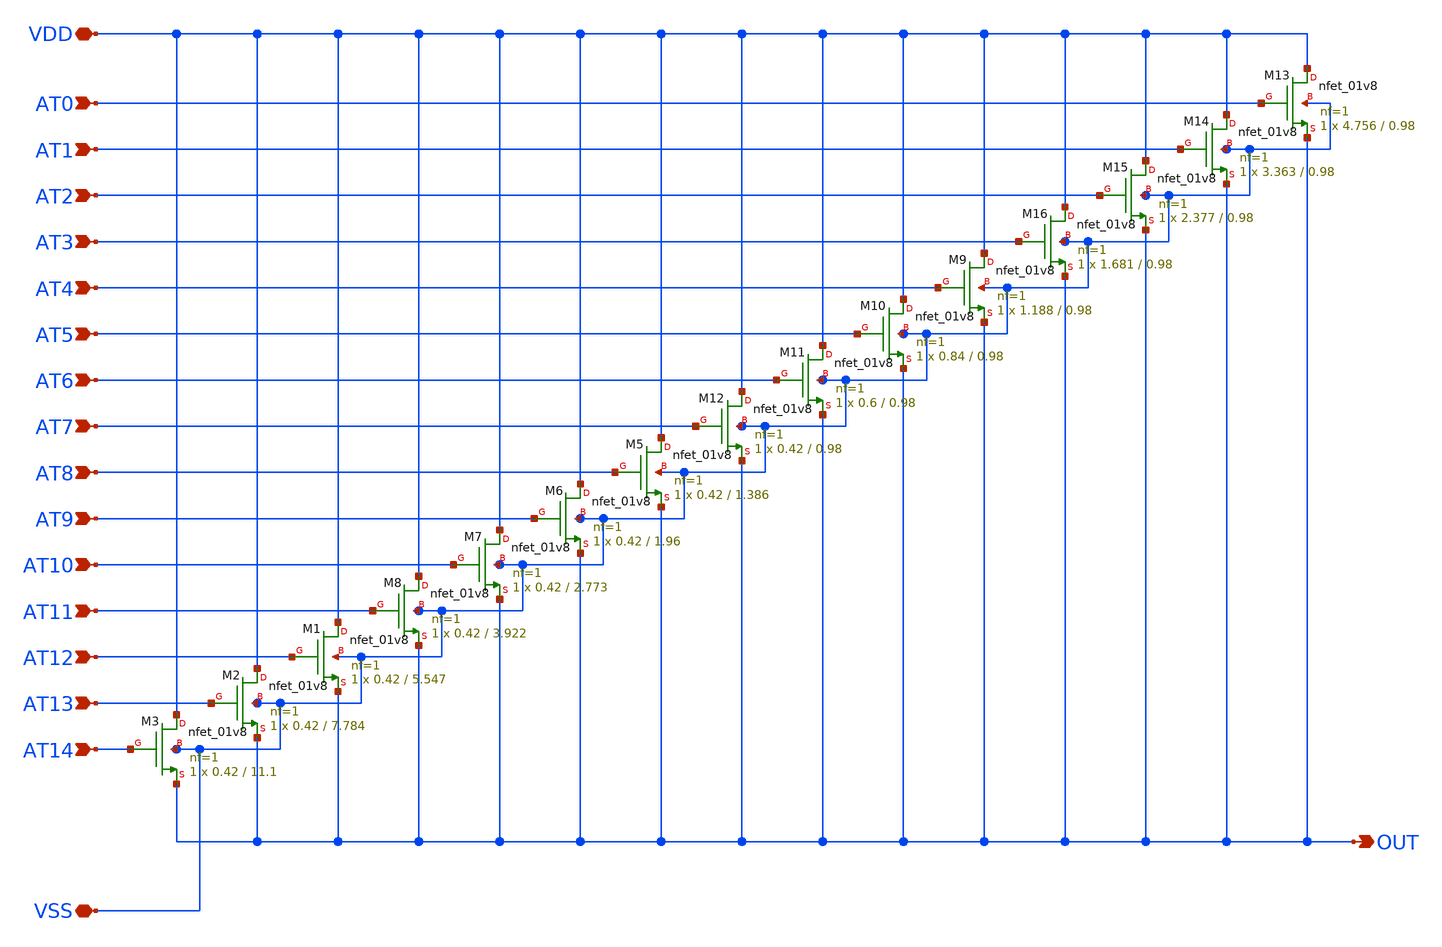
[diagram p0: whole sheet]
** sch_path: xschem/dac_16nfet.sch
**.subckt dac_16nfet AT12 AT13 VDD VSS OUT AT14 AT4 AT5 AT6 AT7 AT8 AT9 AT10 AT11 AT0 AT1 AT2 AT3
*.ipin AT12
*.ipin AT13
*.iopin VDD
*.iopin VSS
*.opin OUT
*.ipin AT14
*.ipin AT4
*.ipin AT5
*.ipin AT6
*.ipin AT7
*.ipin AT8
*.ipin AT9
*.ipin AT10
*.ipin AT11
*.ipin AT0
*.ipin AT1
*.ipin AT2
*.ipin AT3
XM1 VDD AT12 OUT VSS sky130_fd_pr__nfet_01v8 L=5.547 W=0.42 nf=1 ad='int((nf+1)/2) * W/nf * 0.29' as='int((nf+2)/2) * W/nf * 0.29'
+ pd='2*int((nf+1)/2) * (W/nf + 0.29)' ps='2*int((nf+2)/2) * (W/nf + 0.29)' nrd='0.29 / W' nrs='0.29 / W'
+ sa=0 sb=0 sd=0 mult=1 m=1
XM2 VDD AT13 OUT VSS sky130_fd_pr__nfet_01v8 L=7.784 W=0.42 nf=1 ad='int((nf+1)/2) * W/nf * 0.29' as='int((nf+2)/2) * W/nf * 0.29'
+ pd='2*int((nf+1)/2) * (W/nf + 0.29)' ps='2*int((nf+2)/2) * (W/nf + 0.29)' nrd='0.29 / W' nrs='0.29 / W'
+ sa=0 sb=0 sd=0 mult=1 m=1
XM3 VDD AT14 OUT VSS sky130_fd_pr__nfet_01v8 L=11.1 W=0.42 nf=1 ad='int((nf+1)/2) * W/nf * 0.29' as='int((nf+2)/2) * W/nf * 0.29'
+ pd='2*int((nf+1)/2) * (W/nf + 0.29)' ps='2*int((nf+2)/2) * (W/nf + 0.29)' nrd='0.29 / W' nrs='0.29 / W'
+ sa=0 sb=0 sd=0 mult=1 m=1
XM5 VDD AT8 OUT VSS sky130_fd_pr__nfet_01v8 L=1.386 W=0.42 nf=1 ad='int((nf+1)/2) * W/nf * 0.29' as='int((nf+2)/2) * W/nf * 0.29'
+ pd='2*int((nf+1)/2) * (W/nf + 0.29)' ps='2*int((nf+2)/2) * (W/nf + 0.29)' nrd='0.29 / W' nrs='0.29 / W'
+ sa=0 sb=0 sd=0 mult=1 m=1
XM6 VDD AT9 OUT VSS sky130_fd_pr__nfet_01v8 L=1.96 W=0.42 nf=1 ad='int((nf+1)/2) * W/nf * 0.29' as='int((nf+2)/2) * W/nf * 0.29'
+ pd='2*int((nf+1)/2) * (W/nf + 0.29)' ps='2*int((nf+2)/2) * (W/nf + 0.29)' nrd='0.29 / W' nrs='0.29 / W'
+ sa=0 sb=0 sd=0 mult=1 m=1
XM7 VDD AT10 OUT VSS sky130_fd_pr__nfet_01v8 L=2.773 W=0.42 nf=1 ad='int((nf+1)/2) * W/nf * 0.29' as='int((nf+2)/2) * W/nf * 0.29'
+ pd='2*int((nf+1)/2) * (W/nf + 0.29)' ps='2*int((nf+2)/2) * (W/nf + 0.29)' nrd='0.29 / W' nrs='0.29 / W'
+ sa=0 sb=0 sd=0 mult=1 m=1
XM8 VDD AT11 OUT VSS sky130_fd_pr__nfet_01v8 L=3.922 W=0.42 nf=1 ad='int((nf+1)/2) * W/nf * 0.29' as='int((nf+2)/2) * W/nf * 0.29'
+ pd='2*int((nf+1)/2) * (W/nf + 0.29)' ps='2*int((nf+2)/2) * (W/nf + 0.29)' nrd='0.29 / W' nrs='0.29 / W'
+ sa=0 sb=0 sd=0 mult=1 m=1
XM9 VDD AT4 OUT VSS sky130_fd_pr__nfet_01v8 L=0.98 W=1.188 nf=1 ad='int((nf+1)/2) * W/nf * 0.29' as='int((nf+2)/2) * W/nf * 0.29'
+ pd='2*int((nf+1)/2) * (W/nf + 0.29)' ps='2*int((nf+2)/2) * (W/nf + 0.29)' nrd='0.29 / W' nrs='0.29 / W'
+ sa=0 sb=0 sd=0 mult=1 m=1
XM10 VDD AT5 OUT VSS sky130_fd_pr__nfet_01v8 L=0.98 W=0.84 nf=1 ad='int((nf+1)/2) * W/nf * 0.29' as='int((nf+2)/2) * W/nf * 0.29'
+ pd='2*int((nf+1)/2) * (W/nf + 0.29)' ps='2*int((nf+2)/2) * (W/nf + 0.29)' nrd='0.29 / W' nrs='0.29 / W'
+ sa=0 sb=0 sd=0 mult=1 m=1
XM11 VDD AT6 OUT VSS sky130_fd_pr__nfet_01v8 L=0.98 W=0.6 nf=1 ad='int((nf+1)/2) * W/nf * 0.29' as='int((nf+2)/2) * W/nf * 0.29'
+ pd='2*int((nf+1)/2) * (W/nf + 0.29)' ps='2*int((nf+2)/2) * (W/nf + 0.29)' nrd='0.29 / W' nrs='0.29 / W'
+ sa=0 sb=0 sd=0 mult=1 m=1
XM12 VDD AT7 OUT VSS sky130_fd_pr__nfet_01v8 L=0.98 W=0.42 nf=1 ad='int((nf+1)/2) * W/nf * 0.29' as='int((nf+2)/2) * W/nf * 0.29'
+ pd='2*int((nf+1)/2) * (W/nf + 0.29)' ps='2*int((nf+2)/2) * (W/nf + 0.29)' nrd='0.29 / W' nrs='0.29 / W'
+ sa=0 sb=0 sd=0 mult=1 m=1
XM13 VDD AT0 OUT VSS sky130_fd_pr__nfet_01v8 L=0.98 W=4.756 nf=1 ad='int((nf+1)/2) * W/nf * 0.29' as='int((nf+2)/2) * W/nf * 0.29'
+ pd='2*int((nf+1)/2) * (W/nf + 0.29)' ps='2*int((nf+2)/2) * (W/nf + 0.29)' nrd='0.29 / W' nrs='0.29 / W'
+ sa=0 sb=0 sd=0 mult=1 m=1
XM14 VDD AT1 OUT VSS sky130_fd_pr__nfet_01v8 L=0.98 W=3.363 nf=1 ad='int((nf+1)/2) * W/nf * 0.29' as='int((nf+2)/2) * W/nf * 0.29'
+ pd='2*int((nf+1)/2) * (W/nf + 0.29)' ps='2*int((nf+2)/2) * (W/nf + 0.29)' nrd='0.29 / W' nrs='0.29 / W'
+ sa=0 sb=0 sd=0 mult=1 m=1
XM15 VDD AT2 OUT VSS sky130_fd_pr__nfet_01v8 L=0.98 W=2.377 nf=1 ad='int((nf+1)/2) * W/nf * 0.29' as='int((nf+2)/2) * W/nf * 0.29'
+ pd='2*int((nf+1)/2) * (W/nf + 0.29)' ps='2*int((nf+2)/2) * (W/nf + 0.29)' nrd='0.29 / W' nrs='0.29 / W'
+ sa=0 sb=0 sd=0 mult=1 m=1
XM16 VDD AT3 OUT VSS sky130_fd_pr__nfet_01v8 L=0.98 W=1.681 nf=1 ad='int((nf+1)/2) * W/nf * 0.29' as='int((nf+2)/2) * W/nf * 0.29'
+ pd='2*int((nf+1)/2) * (W/nf + 0.29)' ps='2*int((nf+2)/2) * (W/nf + 0.29)' nrd='0.29 / W' nrs='0.29 / W'
+ sa=0 sb=0 sd=0 mult=1 m=1
**.ends
.end
